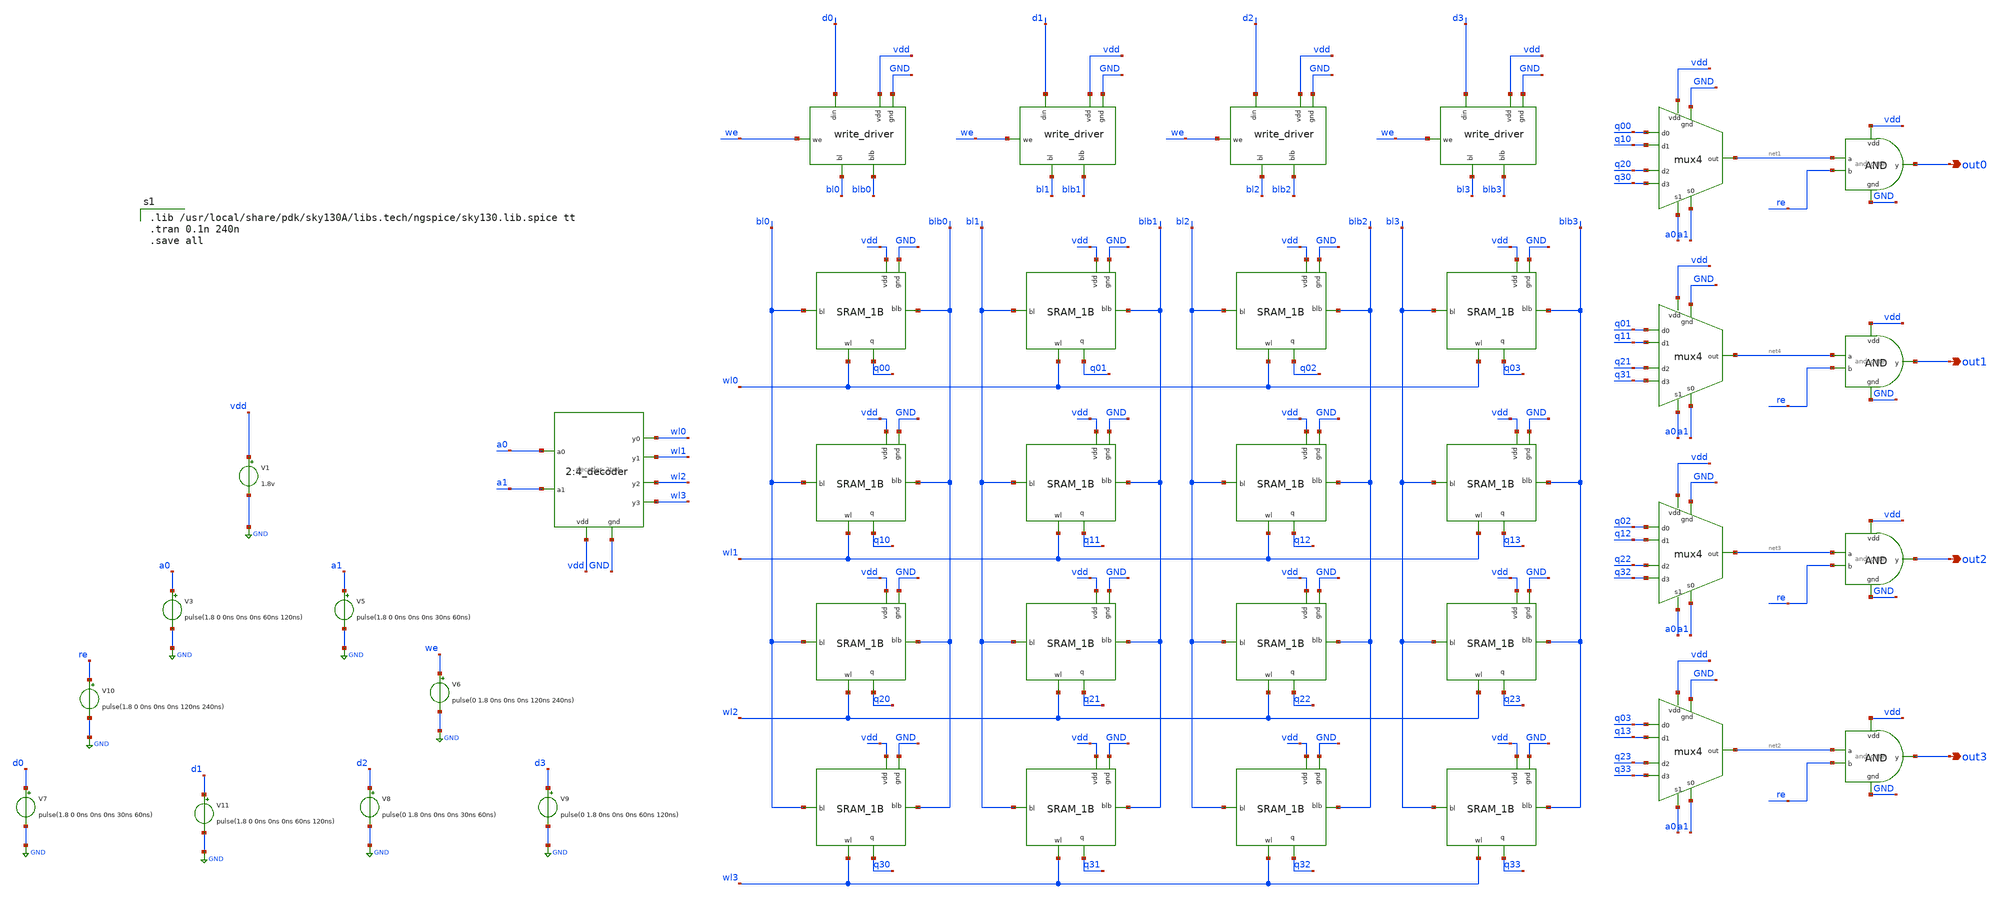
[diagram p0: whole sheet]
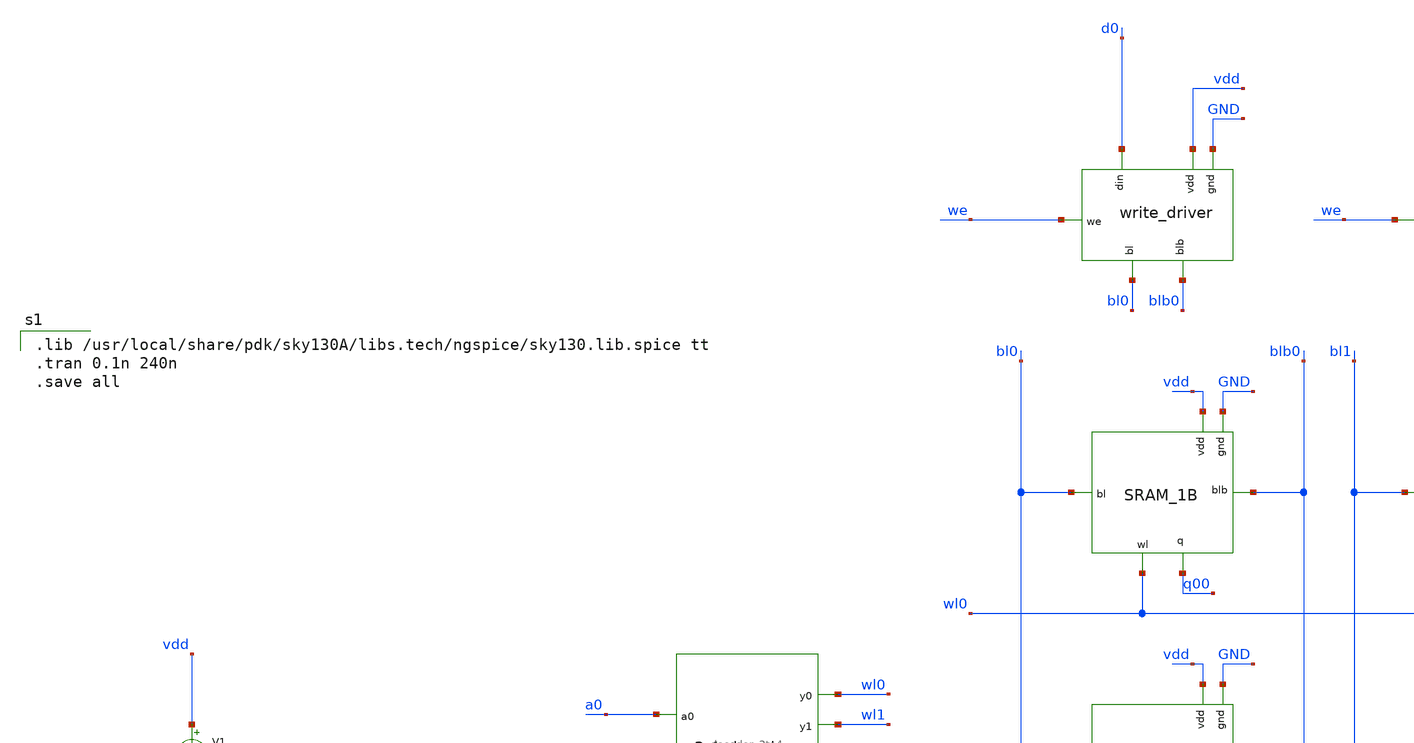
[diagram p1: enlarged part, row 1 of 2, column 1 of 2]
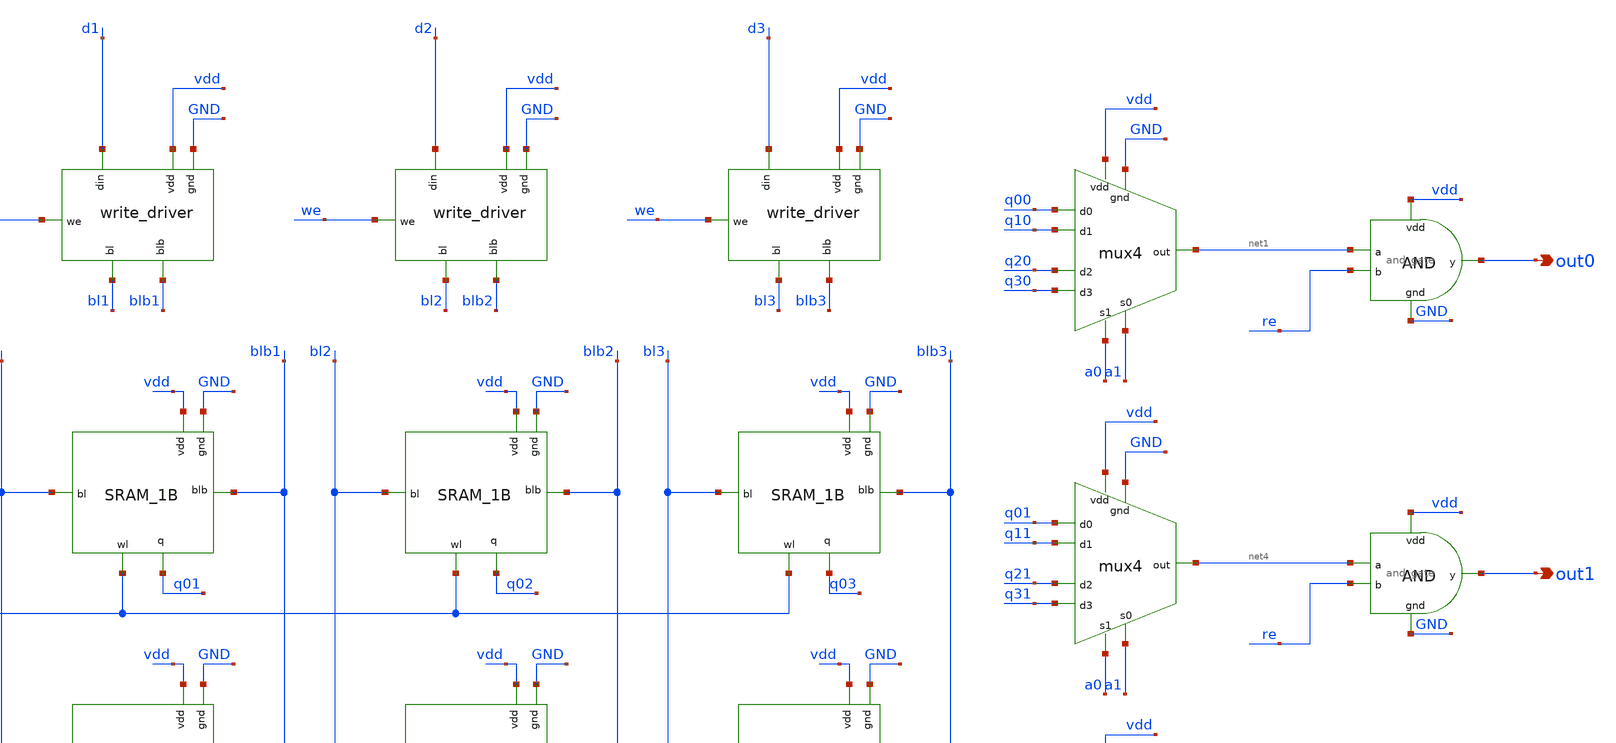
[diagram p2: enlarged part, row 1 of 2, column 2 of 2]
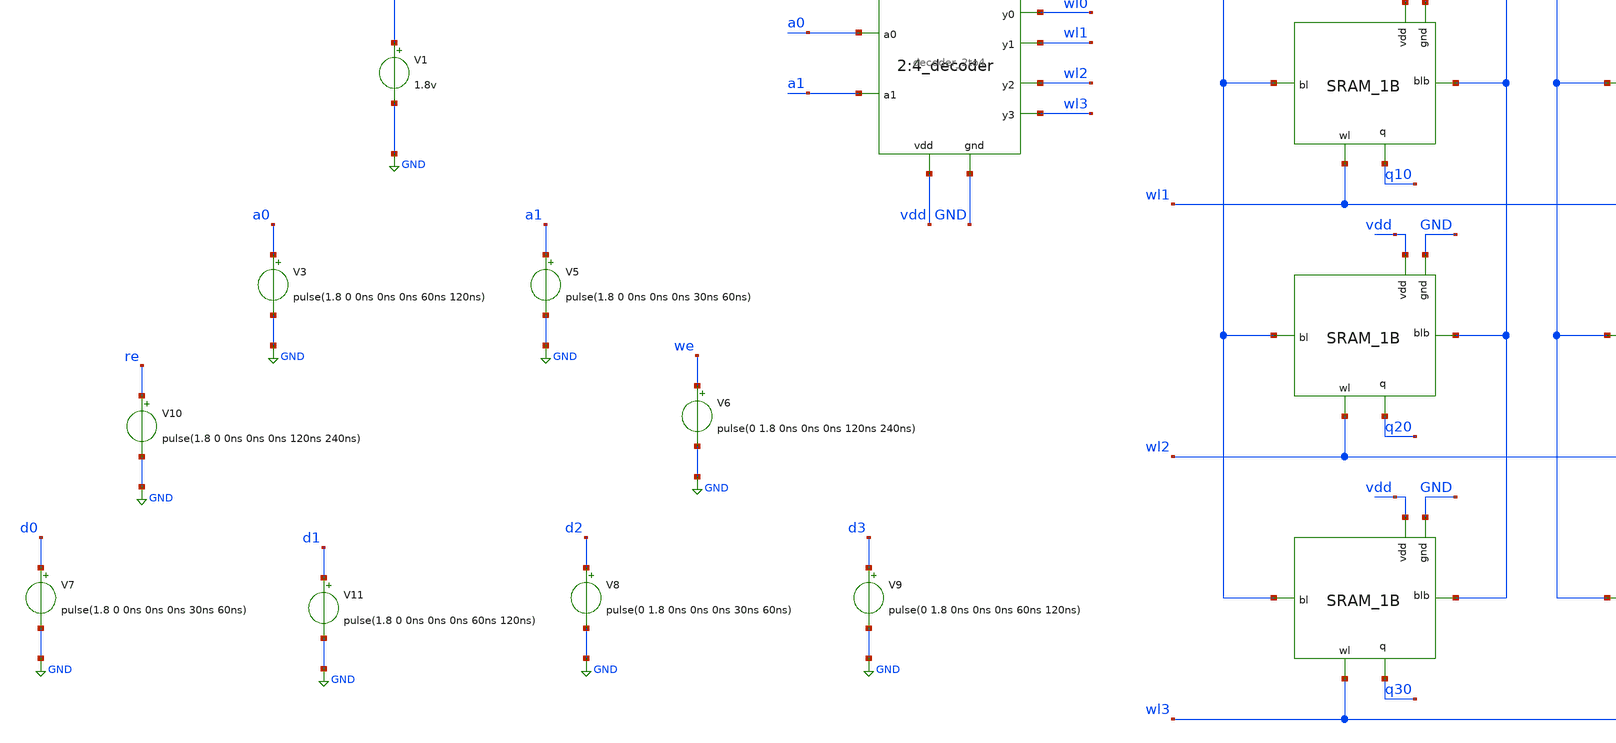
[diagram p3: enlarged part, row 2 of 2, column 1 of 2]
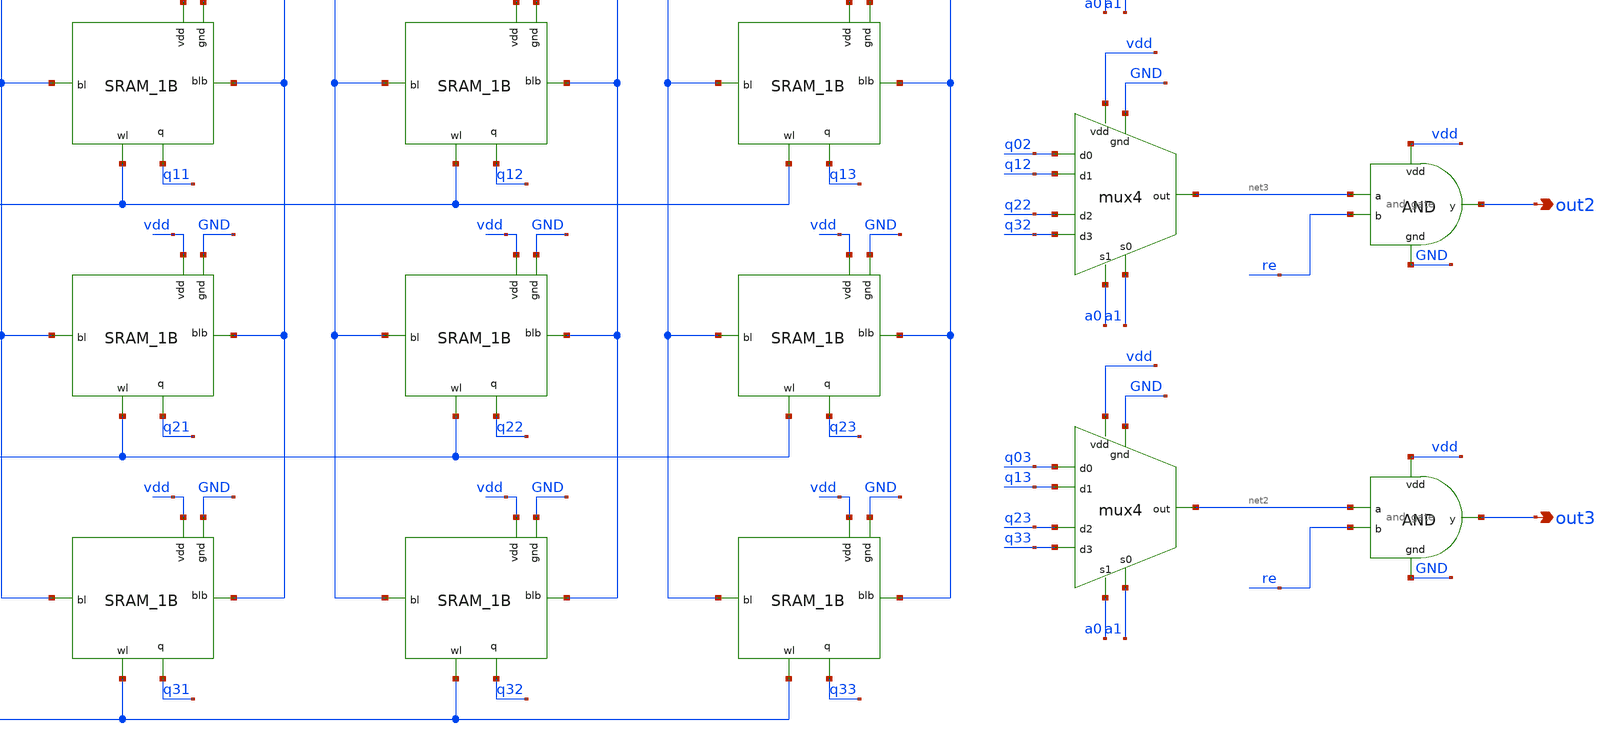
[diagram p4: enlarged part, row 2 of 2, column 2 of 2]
** sch_path: sram/4x4_nopch.sch
**.subckt 4x4_nopch out0 out1 out2 out3
*.opin out0
*.opin out1
*.opin out2
*.opin out3
x2 wl0 vdd GND a0 a1 wl1 wl2 wl3 decoder_2to4
x3 vdd GND d0 bl0 blb0 we write_driver
x21 vdd GND d1 bl1 blb1 we write_driver
x22 vdd GND d2 bl2 blb2 we write_driver
x23 vdd GND d3 bl3 blb3 we write_driver
V1 vdd GND 1.8v
V3 a0 GND pulse(1.8 0 0ns 0ns 0ns 60ns 120ns)
V5 a1 GND pulse(1.8 0 0ns 0ns 0ns 30ns 60ns)
V6 we GND pulse(0 1.8 0ns 0ns 0ns 120ns 240ns)
V7 d0 GND pulse(1.8 0 0ns 0ns 0ns 30ns 60ns)
V11 d1 GND pulse(1.8 0 0ns 0ns 0ns 60ns 120ns)
V8 d2 GND pulse(0 1.8 0ns 0ns 0ns 30ns 60ns)
V9 d3 GND pulse(0 1.8 0ns 0ns 0ns 60ns 120ns)
V10 re GND pulse(1.8 0 0ns 0ns 0ns 120ns 240ns)
x19 vdd GND q00 q10 net1 a0 q20 q30 a1 mux4
x20 vdd GND q01 q11 net4 a0 q21 q31 a1 mux4
x24 vdd GND q02 q12 net3 a0 q22 q32 a1 mux4
x25 vdd GND q03 q13 net2 a0 q23 q33 a1 mux4
x26 vdd net1 out0 re GND and_gate
x27 vdd net4 out1 re GND and_gate
x28 vdd net3 out2 re GND and_gate
x29 vdd net2 out3 re GND and_gate
x1 wl0 vdd blb0 bl0 q00 GND sram_1b
x4 wl0 vdd blb1 bl1 q01 GND sram_1b
x5 wl0 vdd blb2 bl2 q02 GND sram_1b
x6 wl0 vdd blb3 bl3 q03 GND sram_1b
x7 wl1 vdd blb3 bl3 q13 GND sram_1b
x8 wl1 vdd blb2 bl2 q12 GND sram_1b
x9 wl1 vdd blb1 bl1 q11 GND sram_1b
x10 wl1 vdd blb0 bl0 q10 GND sram_1b
x11 wl2 vdd blb0 bl0 q20 GND sram_1b
x12 wl2 vdd blb1 bl1 q21 GND sram_1b
x13 wl2 vdd blb2 bl2 q22 GND sram_1b
x14 wl2 vdd blb3 bl3 q23 GND sram_1b
x15 wl3 vdd blb3 bl3 q33 GND sram_1b
x16 wl3 vdd blb2 bl2 q32 GND sram_1b
x17 wl3 vdd blb1 bl1 q31 GND sram_1b
x18 wl3 vdd blb0 bl0 q30 GND sram_1b
**** begin user architecture code

.lib /usr/local/share/pdk/sky130A/libs.tech/ngspice/sky130.lib.spice tt
.tran 0.1n 240n
.save all

**** end user architecture code
**.ends

* expanding   symbol:  decoder_2to4.sym # of pins=8
** sym_path: sram/decoder_2to4.sym
** sch_path: sram/decoder_2to4.sch
.subckt decoder_2to4 y0 vdd gnd a0 a1 y1 y2 y3
*.opin y0
*.opin y1
*.opin y2
*.opin y3
*.ipin vdd
*.ipin gnd
*.ipin a0
*.ipin a1
x1 vdd a0b y0 a1b gnd and_gate
x2 vdd a0 a0b gnd inverter
x3 vdd a0b y1 a1 gnd and_gate
x4 vdd a0 y2 a1b gnd and_gate
x5 vdd a0 y3 a1 gnd and_gate
x6 vdd a1 a1b gnd inverter
.ends


* expanding   symbol:  write_driver.sym # of pins=6
** sym_path: sram/write_driver.sym
** sch_path: sram/write_driver.sch
.subckt write_driver vdd gnd din bl blb we
*.ipin din
*.ipin we
*.opin bl
*.opin blb
*.ipin vdd
*.ipin gnd
XM1 net2 web vdd vdd sky130_fd_pr__pfet_01v8 L=0.15 W=1 nf=1 ad='int((nf+1)/2) * W/nf * 0.29' as='int((nf+2)/2) * W/nf * 0.29'
+ pd='2*int((nf+1)/2) * (W/nf + 0.29)' ps='2*int((nf+2)/2) * (W/nf + 0.29)' nrd='0.29 / W' nrs='0.29 / W'
+ sa=0 sb=0 sd=0 mult=1 m=1
XM2 blb din net1 blb sky130_fd_pr__nfet_01v8 L=0.15 W=1 nf=1 ad='int((nf+1)/2) * W/nf * 0.29' as='int((nf+2)/2) * W/nf * 0.29'
+ pd='2*int((nf+1)/2) * (W/nf + 0.29)' ps='2*int((nf+2)/2) * (W/nf + 0.29)' nrd='0.29 / W' nrs='0.29 / W'
+ sa=0 sb=0 sd=0 mult=1 m=1
XM3 blb din net2 net2 sky130_fd_pr__pfet_01v8 L=0.15 W=1 nf=1 ad='int((nf+1)/2) * W/nf * 0.29' as='int((nf+2)/2) * W/nf * 0.29'
+ pd='2*int((nf+1)/2) * (W/nf + 0.29)' ps='2*int((nf+2)/2) * (W/nf + 0.29)' nrd='0.29 / W' nrs='0.29 / W'
+ sa=0 sb=0 sd=0 mult=1 m=1
XM4 net1 we gnd net1 sky130_fd_pr__nfet_01v8 L=0.15 W=1 nf=1 ad='int((nf+1)/2) * W/nf * 0.29' as='int((nf+2)/2) * W/nf * 0.29'
+ pd='2*int((nf+1)/2) * (W/nf + 0.29)' ps='2*int((nf+2)/2) * (W/nf + 0.29)' nrd='0.29 / W' nrs='0.29 / W'
+ sa=0 sb=0 sd=0 mult=1 m=1
XM5 net4 web vdd vdd sky130_fd_pr__pfet_01v8 L=0.15 W=1 nf=1 ad='int((nf+1)/2) * W/nf * 0.29' as='int((nf+2)/2) * W/nf * 0.29'
+ pd='2*int((nf+1)/2) * (W/nf + 0.29)' ps='2*int((nf+2)/2) * (W/nf + 0.29)' nrd='0.29 / W' nrs='0.29 / W'
+ sa=0 sb=0 sd=0 mult=1 m=1
XM6 bl dinb net3 net3 sky130_fd_pr__nfet_01v8 L=0.15 W=1 nf=1 ad='int((nf+1)/2) * W/nf * 0.29' as='int((nf+2)/2) * W/nf * 0.29'
+ pd='2*int((nf+1)/2) * (W/nf + 0.29)' ps='2*int((nf+2)/2) * (W/nf + 0.29)' nrd='0.29 / W' nrs='0.29 / W'
+ sa=0 sb=0 sd=0 mult=1 m=1
XM7 bl dinb net4 net4 sky130_fd_pr__pfet_01v8 L=0.15 W=1 nf=1 ad='int((nf+1)/2) * W/nf * 0.29' as='int((nf+2)/2) * W/nf * 0.29'
+ pd='2*int((nf+1)/2) * (W/nf + 0.29)' ps='2*int((nf+2)/2) * (W/nf + 0.29)' nrd='0.29 / W' nrs='0.29 / W'
+ sa=0 sb=0 sd=0 mult=1 m=1
XM8 net3 we gnd gnd sky130_fd_pr__nfet_01v8 L=0.15 W=1 nf=1 ad='int((nf+1)/2) * W/nf * 0.29' as='int((nf+2)/2) * W/nf * 0.29'
+ pd='2*int((nf+1)/2) * (W/nf + 0.29)' ps='2*int((nf+2)/2) * (W/nf + 0.29)' nrd='0.29 / W' nrs='0.29 / W'
+ sa=0 sb=0 sd=0 mult=1 m=1
x1 vdd din dinb gnd inverter
x2 vdd we web gnd inverter
.ends


* expanding   symbol:  mux4.sym # of pins=9
** sym_path: sram/mux4.sym
** sch_path: sram/mux4.sch
.subckt mux4 vdd gnd d0 d1 out s1 d2 d3 s0
*.ipin d0
*.ipin d1
*.ipin d2
*.ipin d3
*.ipin s0
*.ipin s1
*.opin out
*.ipin vdd
*.ipin gnd
x1 d0 s0 vdd gnd net1 d1 mux2_tg
x2 d2 s0 vdd gnd net2 d3 mux2_tg
x3 net1 s1 vdd gnd out net2 mux2_tg
.ends


* expanding   symbol:  and_gate.sym # of pins=5
** sym_path: sram/and_gate.sym
** sch_path: sram/and_gate.sch
.subckt and_gate vdd a y b gnd
*.ipin a
*.ipin b
*.ipin vdd
*.ipin gnd
*.opin y
x2 vdd net1 y gnd inverter
x1 vdd a b gnd net1 nand_gate
.ends


* expanding   symbol:  sram_1b.sym # of pins=6
** sym_path: sram/sram_1b.sym
** sch_path: sram/sram_1b.sch
.subckt sram_1b wl vdd blb bl q gnd
*.ipin gnd
*.ipin bl
*.ipin blb
*.ipin vdd
*.ipin wl
*.opin q
XM1 blb wl net1 gnd sky130_fd_pr__nfet_01v8 L=0.15 W=1 nf=1 ad='int((nf+1)/2) * W/nf * 0.29' as='int((nf+2)/2) * W/nf * 0.29'
+ pd='2*int((nf+1)/2) * (W/nf + 0.29)' ps='2*int((nf+2)/2) * (W/nf + 0.29)' nrd='0.29 / W' nrs='0.29 / W'
+ sa=0 sb=0 sd=0 mult=1 m=1
XM3 q wl bl gnd sky130_fd_pr__nfet_01v8 L=0.15 W=1 nf=1 ad='int((nf+1)/2) * W/nf * 0.29' as='int((nf+2)/2) * W/nf * 0.29'
+ pd='2*int((nf+1)/2) * (W/nf + 0.29)' ps='2*int((nf+2)/2) * (W/nf + 0.29)' nrd='0.29 / W' nrs='0.29 / W'
+ sa=0 sb=0 sd=0 mult=1 m=1
XM5 q net1 vdd vdd sky130_fd_pr__pfet_01v8 L=0.15 W=1 nf=1 ad='int((nf+1)/2) * W/nf * 0.29' as='int((nf+2)/2) * W/nf * 0.29'
+ pd='2*int((nf+1)/2) * (W/nf + 0.29)' ps='2*int((nf+2)/2) * (W/nf + 0.29)' nrd='0.29 / W' nrs='0.29 / W'
+ sa=0 sb=0 sd=0 mult=1 m=1
XM6 net1 q vdd vdd sky130_fd_pr__pfet_01v8 L=0.15 W=1 nf=1 ad='int((nf+1)/2) * W/nf * 0.29' as='int((nf+2)/2) * W/nf * 0.29'
+ pd='2*int((nf+1)/2) * (W/nf + 0.29)' ps='2*int((nf+2)/2) * (W/nf + 0.29)' nrd='0.29 / W' nrs='0.29 / W'
+ sa=0 sb=0 sd=0 mult=1 m=1
XM2 net1 q gnd gnd sky130_fd_pr__nfet_01v8 L=0.15 W=1 nf=1 ad='int((nf+1)/2) * W/nf * 0.29' as='int((nf+2)/2) * W/nf * 0.29'
+ pd='2*int((nf+1)/2) * (W/nf + 0.29)' ps='2*int((nf+2)/2) * (W/nf + 0.29)' nrd='0.29 / W' nrs='0.29 / W'
+ sa=0 sb=0 sd=0 mult=1 m=1
XM4 q net1 gnd gnd sky130_fd_pr__nfet_01v8 L=0.15 W=1 nf=1 ad='int((nf+1)/2) * W/nf * 0.29' as='int((nf+2)/2) * W/nf * 0.29'
+ pd='2*int((nf+1)/2) * (W/nf + 0.29)' ps='2*int((nf+2)/2) * (W/nf + 0.29)' nrd='0.29 / W' nrs='0.29 / W'
+ sa=0 sb=0 sd=0 mult=1 m=1
.ends


* expanding   symbol:  inverter.sym # of pins=4
** sym_path: sram/inverter.sym
** sch_path: sram/inverter.sch
.subckt inverter vdd vin vout gnd
*.ipin vin
*.ipin vdd
*.ipin gnd
*.opin vout
XM1 vout vin gnd gnd sky130_fd_pr__nfet_01v8 L=0.15 W=1 nf=1 ad='int((nf+1)/2) * W/nf * 0.29' as='int((nf+2)/2) * W/nf * 0.29'
+ pd='2*int((nf+1)/2) * (W/nf + 0.29)' ps='2*int((nf+2)/2) * (W/nf + 0.29)' nrd='0.29 / W' nrs='0.29 / W'
+ sa=0 sb=0 sd=0 mult=1 m=1
XM2 vout vin vdd vdd sky130_fd_pr__pfet_01v8 L=0.15 W=1 nf=1 ad='int((nf+1)/2) * W/nf * 0.29' as='int((nf+2)/2) * W/nf * 0.29'
+ pd='2*int((nf+1)/2) * (W/nf + 0.29)' ps='2*int((nf+2)/2) * (W/nf + 0.29)' nrd='0.29 / W' nrs='0.29 / W'
+ sa=0 sb=0 sd=0 mult=1 m=1
.ends


* expanding   symbol:  mux2_tg.sym # of pins=6
** sym_path: sram/mux2_tg.sym
** sch_path: sram/mux2_tg.sch
.subckt mux2_tg in0 c vdd gnd y in1
*.ipin in0
*.ipin in1
*.ipin c
*.opin y
*.ipin vdd
*.ipin gnd
XM5 y c in0 vdd sky130_fd_pr__pfet_01v8 L=0.15 W=1 nf=1 ad='int((nf+1)/2) * W/nf * 0.29' as='int((nf+2)/2) * W/nf * 0.29'
+ pd='2*int((nf+1)/2) * (W/nf + 0.29)' ps='2*int((nf+2)/2) * (W/nf + 0.29)' nrd='0.29 / W' nrs='0.29 / W'
+ sa=0 sb=0 sd=0 mult=1 m=1
XM2 in0 cb y gnd sky130_fd_pr__nfet_01v8 L=0.15 W=1 nf=1 ad='int((nf+1)/2) * W/nf * 0.29' as='int((nf+2)/2) * W/nf * 0.29'
+ pd='2*int((nf+1)/2) * (W/nf + 0.29)' ps='2*int((nf+2)/2) * (W/nf + 0.29)' nrd='0.29 / W' nrs='0.29 / W'
+ sa=0 sb=0 sd=0 mult=1 m=1
XM1 y cb in1 vdd sky130_fd_pr__pfet_01v8 L=0.15 W=1 nf=1 ad='int((nf+1)/2) * W/nf * 0.29' as='int((nf+2)/2) * W/nf * 0.29'
+ pd='2*int((nf+1)/2) * (W/nf + 0.29)' ps='2*int((nf+2)/2) * (W/nf + 0.29)' nrd='0.29 / W' nrs='0.29 / W'
+ sa=0 sb=0 sd=0 mult=1 m=1
XM3 in1 c y gnd sky130_fd_pr__nfet_01v8 L=0.15 W=1 nf=1 ad='int((nf+1)/2) * W/nf * 0.29' as='int((nf+2)/2) * W/nf * 0.29'
+ pd='2*int((nf+1)/2) * (W/nf + 0.29)' ps='2*int((nf+2)/2) * (W/nf + 0.29)' nrd='0.29 / W' nrs='0.29 / W'
+ sa=0 sb=0 sd=0 mult=1 m=1
x1 vdd c cb gnd inverter
.ends


* expanding   symbol:  nand_gate.sym # of pins=5
** sym_path: sram/nand_gate.sym
** sch_path: sram/nand_gate.sch
.subckt nand_gate vdd a b gnd y
*.ipin a
*.ipin b
*.ipin vdd
*.ipin gnd
*.opin y
XM1 y a vdd vdd sky130_fd_pr__pfet_01v8 L=0.15 W=1 nf=1 ad='int((nf+1)/2) * W/nf * 0.29' as='int((nf+2)/2) * W/nf * 0.29'
+ pd='2*int((nf+1)/2) * (W/nf + 0.29)' ps='2*int((nf+2)/2) * (W/nf + 0.29)' nrd='0.29 / W' nrs='0.29 / W'
+ sa=0 sb=0 sd=0 mult=1 m=1
XM2 y a net1 net1 sky130_fd_pr__nfet_01v8 L=0.15 W=1 nf=1 ad='int((nf+1)/2) * W/nf * 0.29' as='int((nf+2)/2) * W/nf * 0.29'
+ pd='2*int((nf+1)/2) * (W/nf + 0.29)' ps='2*int((nf+2)/2) * (W/nf + 0.29)' nrd='0.29 / W' nrs='0.29 / W'
+ sa=0 sb=0 sd=0 mult=1 m=1
XM3 y b vdd vdd sky130_fd_pr__pfet_01v8 L=0.15 W=1 nf=1 ad='int((nf+1)/2) * W/nf * 0.29' as='int((nf+2)/2) * W/nf * 0.29'
+ pd='2*int((nf+1)/2) * (W/nf + 0.29)' ps='2*int((nf+2)/2) * (W/nf + 0.29)' nrd='0.29 / W' nrs='0.29 / W'
+ sa=0 sb=0 sd=0 mult=1 m=1
XM4 net1 b gnd gnd sky130_fd_pr__nfet_01v8 L=0.15 W=1 nf=1 ad='int((nf+1)/2) * W/nf * 0.29' as='int((nf+2)/2) * W/nf * 0.29'
+ pd='2*int((nf+1)/2) * (W/nf + 0.29)' ps='2*int((nf+2)/2) * (W/nf + 0.29)' nrd='0.29 / W' nrs='0.29 / W'
+ sa=0 sb=0 sd=0 mult=1 m=1
.ends

.GLOBAL GND
.end
